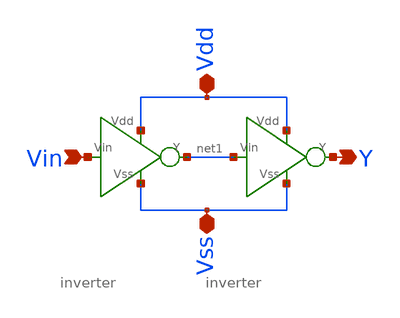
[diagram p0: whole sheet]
** sch_path: buffer/buffer.sch
**.subckt buffer Vdd Vss Vin Y
*.iopin Vdd
*.iopin Vss
*.ipin Vin
*.opin Y
x1 Vss Vin Vdd net1 inverter
x2 Vss net1 Vdd Y inverter
**.ends
.end
